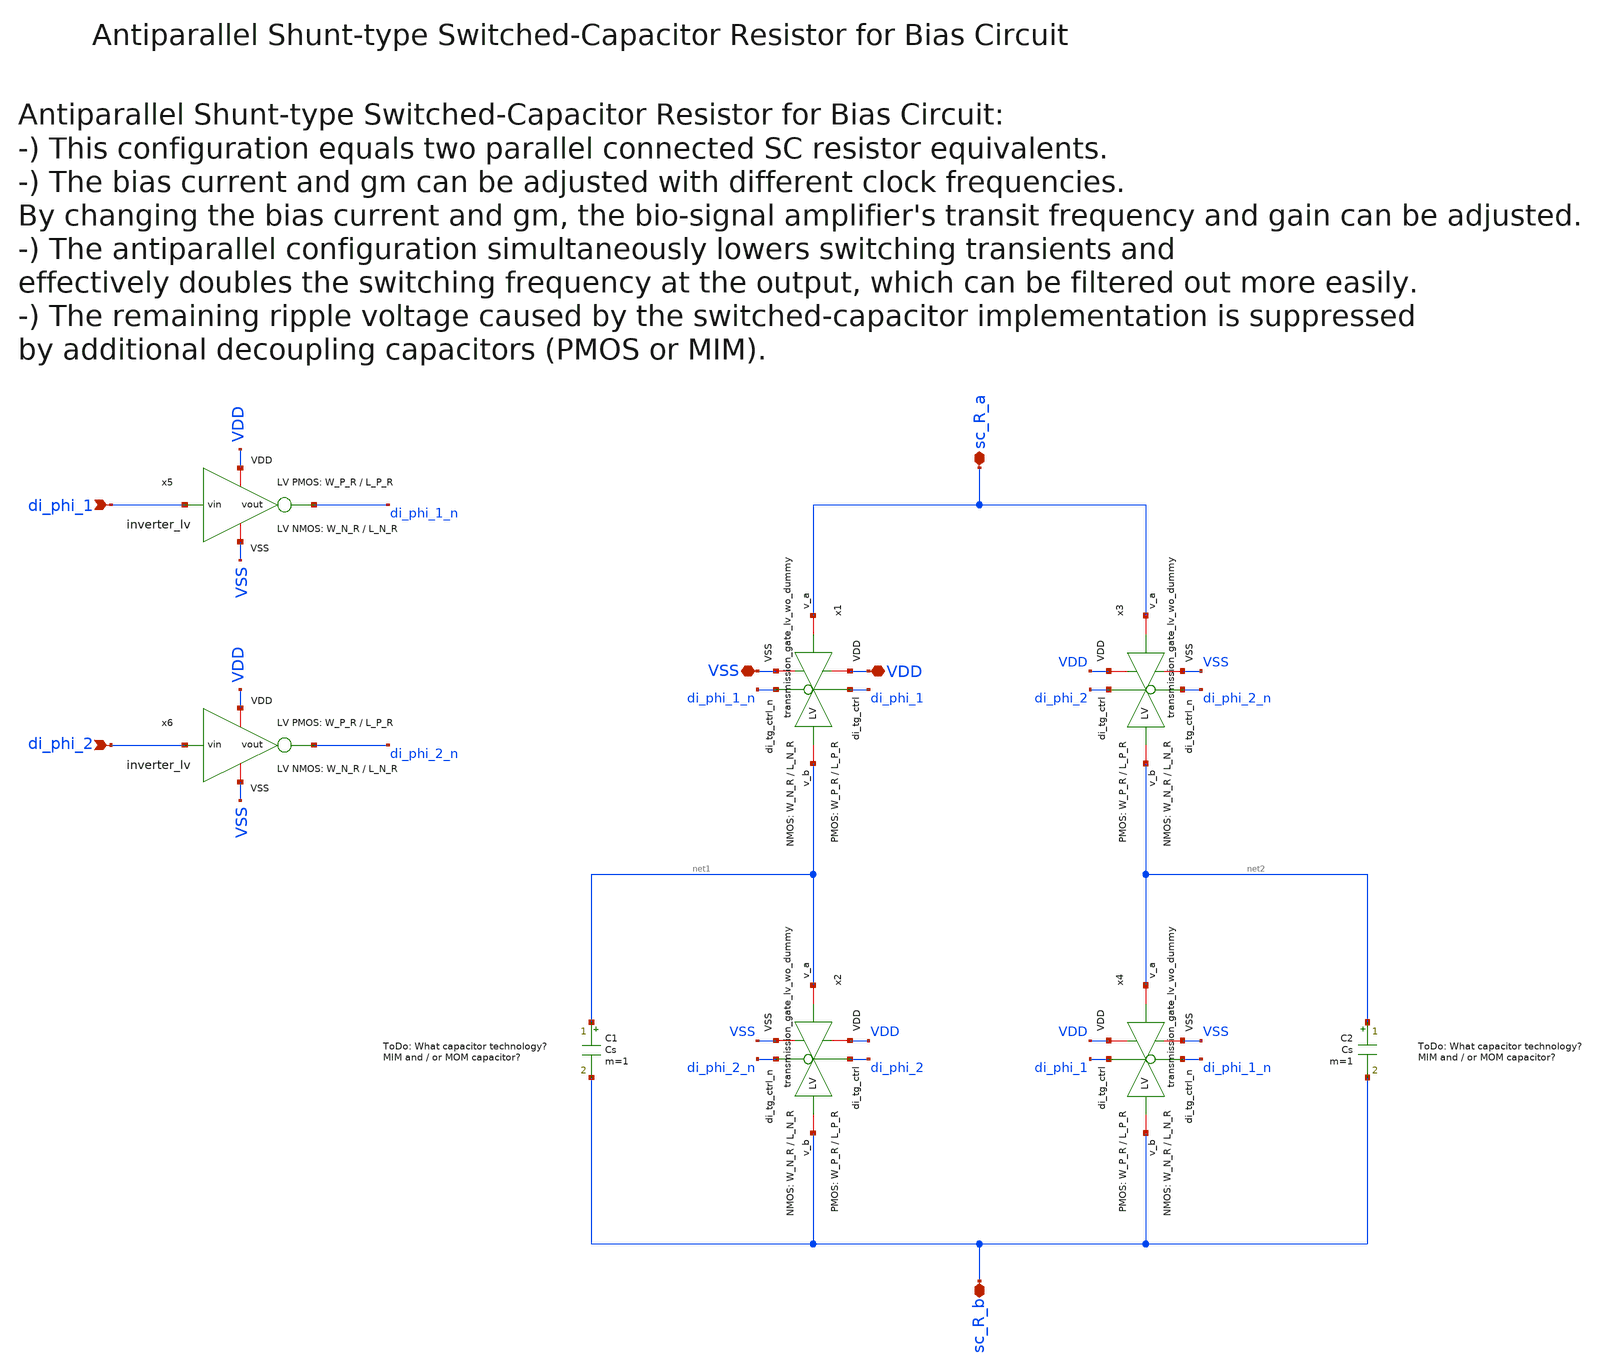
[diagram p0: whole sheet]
** sch_path: SG13G2_ATBS-ADC-main/xschem/bio_amplifier/amplifier_core/bias_circuit/sc_bias_resistor/sc_bias_resistor.sch
**.subckt sc_bias_resistor VSS VDD sc_R_a sc_R_b di_phi_1 di_phi_2
*.iopin VSS
*.iopin VDD
*.iopin sc_R_a
*.iopin sc_R_b
*.ipin di_phi_1
*.ipin di_phi_2
C1 net1 sc_R_b Cs m=1
x1 VDD di_phi_1 VSS net1 sc_R_a di_phi_1_n transmission_gate_lv_wo_dummy W_P=W_P_R L_P=L_P_R
+ W_N=W_N_R L_N=L_N_R
x2 VDD di_phi_2 VSS sc_R_b net1 di_phi_2_n transmission_gate_lv_wo_dummy W_P=W_P_R L_P=L_P_R
+ W_N=W_N_R L_N=L_N_R
C2 net2 sc_R_b Cs m=1
x3 VDD di_phi_2 VSS net2 sc_R_a di_phi_2_n transmission_gate_lv_wo_dummy W_P=W_P_R L_P=L_P_R
+ W_N=W_N_R L_N=L_N_R
x4 VDD di_phi_1 VSS sc_R_b net2 di_phi_1_n transmission_gate_lv_wo_dummy W_P=W_P_R L_P=L_P_R
+ W_N=W_N_R L_N=L_N_R
x5 VDD di_phi_1 di_phi_1_n VSS inverter_lv W_P=W_P_R L_P=L_P_R W_N=W_N_R L_N=L_N_R
x6 VDD di_phi_2 di_phi_2_n VSS inverter_lv W_P=W_P_R L_P=L_P_R W_N=W_N_R L_N=L_N_R
**.ends

* expanding   symbol:  transmission_gate/transmission_gate_lv_wo_dummy.sym # of pins=6
** sym_path: SG13G2_ATBS-ADC-main/xschem/transmission_gate/transmission_gate_lv_wo_dummy.sym
** sch_path: SG13G2_ATBS-ADC-main/xschem/transmission_gate/transmission_gate_lv_wo_dummy.sch
.subckt transmission_gate_lv_wo_dummy VDD di_tg_ctrl VSS v_b v_a di_tg_ctrl_n  W_P=1.0u L_P=0.13u
+ W_N=1.0u L_N=0.13u
*.iopin v_a
*.iopin v_b
*.iopin VDD
*.iopin VSS
*.ipin di_tg_ctrl
*.ipin di_tg_ctrl_n
XM1 v_a di_tg_ctrl v_b VSS sg13_lv_nmos w=W_N l=L_N ng=1 m=1 mm_ok=1
XM2 v_a di_tg_ctrl_n v_b VDD sg13_lv_pmos w=W_P l=L_P ng=1 m=1 mm_ok=1
.ends


* expanding   symbol:  inverter/inverter_lv.sym # of pins=4
** sym_path: SG13G2_ATBS-ADC-main/xschem/inverter/inverter_lv.sym
** sch_path: SG13G2_ATBS-ADC-main/xschem/inverter/inverter_lv.sch
.subckt inverter_lv VDD vin vout VSS  W_P=3.0u L_P=0.13u W_N=1.0u L_N=0.13u
*.ipin vin
*.iopin VDD
*.iopin VSS
*.opin vout
XM1 vout vin VDD VDD sg13_lv_pmos w=W_P l=L_P ng=1 m=1 mm_ok=1
XM2 vout vin VSS VSS sg13_lv_nmos w=W_N l=L_N ng=1 m=1 mm_ok=1
.ends

.end
